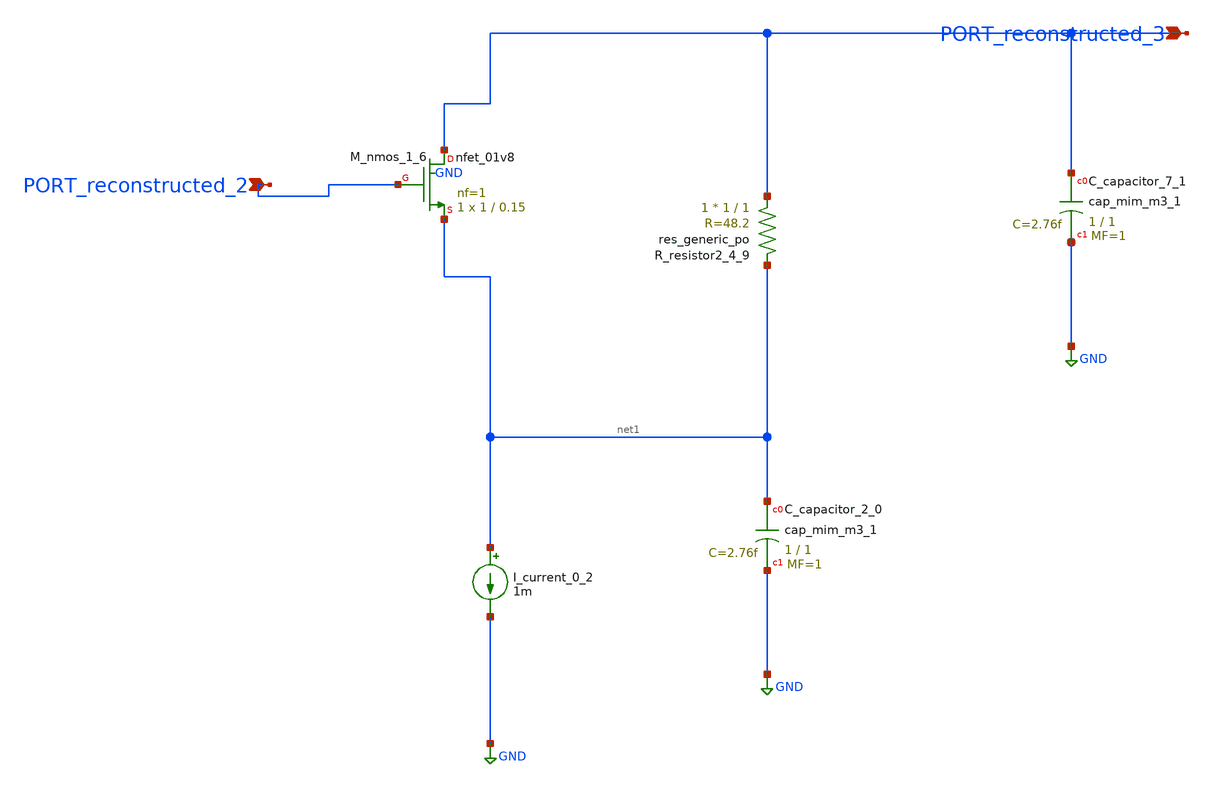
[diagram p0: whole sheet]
** sch_path: schematics/AMSNet/383.sch
**.subckt 383 PORT_reconstructed_2 PORT_reconstructed_3
*.ipin PORT_reconstructed_2
*.ipin PORT_reconstructed_3
XC_capacitor_2_0 net1 GND sky130_fd_pr__cap_mim_m3_1 W=1 L=1 MF=1 m=1
XC_capacitor_7_1 PORT_reconstructed_3 GND sky130_fd_pr__cap_mim_m3_1 W=1 L=1 MF=1 m=1
I_current_0_2 net1 GND 1m
XM_nmos_1_6 PORT_reconstructed_3 PORT_reconstructed_2 net1 GND sky130_fd_pr__nfet_01v8 L=0.15 W=1 nf=1
+ ad='int((1 + 1)/2) * 1 / 1 * 0.29' as='int((1 + 2)/2) * 1 / 1 * 0.29' pd='2*int((1 + 1)/2) * (1 / 1 + 0.29)'
+ ps='2*int((1 + 2)/2) * (1 / 1 + 0.29)' nrd='0.29 / 1 ' nrs='0.29 / 1 ' sa=0 sb=0 sd=0 mult=1 m=1
XR_resistor2_4_9 PORT_reconstructed_3 net1 sky130_fd_pr__res_generic_po W=1 L=1 m=1
**.ends
.GLOBAL GND
.end
